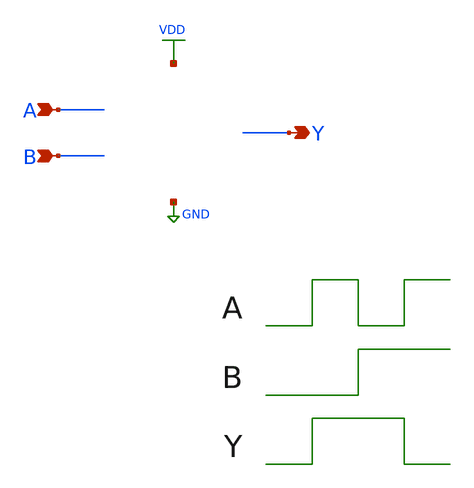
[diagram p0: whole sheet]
** sch_path: xor_test.sch
**.subckt xor_test A B Y
*.ipin A
*.ipin B
*.opin Y
**** begin user architecture code



VP VDD 0 dc 1.8

// XOR_A TEST

VA A 0 dc 0
VB B 0 dc 1.8

.control
save a b c d y
alter @va[PULSE] [ 1.8 0 1n 40p 40p 10n 20n ]
alter @vb[PULSE] [ 1.8 0 1n 40p 40p 20n 40n ]
tran 10p 60n
meas tran test1 FIND v(y) WHEN time=5n > NUL
meas tran test2 FIND v(y) WHEN time=15n > NUL
meas tran test3 FIND v(y) WHEN time=25n > NUL
meas tran test4 FIND v(y) WHEN time=35n > NUL
echo '*** TEST ***'
echo '-B--A--Y-'
echo -n '-L--L--'
if test1 >= 0.9
  echo 'H-'
else
  echo 'L-'
end
echo -n '-L--H--'
if test2 >= 0.9
  echo 'H-'
else
  echo 'L-'
end
echo -n '-H--L--'
if test3 >= 0.9
  echo 'H-'
else
  echo 'L-'
end
echo -n '-H--H--'
if test4 >= 0.9
  echo 'H-'
else
  echo 'L-'
end
.endc



 .param mc_mm_switch=0
.param mc_pr_switch=0
.include $::SKYWATER_MODELS/corners/tt.spice
.include $::SKYWATER_MODELS/r+c/res_typical__cap_typical.spice
.include $::SKYWATER_MODELS/r+c/res_typical__cap_typical__lin.spice
.include $::SKYWATER_MODELS/corners/tt/specialized_cells.spice
.include $::SKYWATER_STDCELLS/sky130_fd_sc_hd.spice

**** end user architecture code
**.ends
.GLOBAL VDD
.GLOBAL GND
.end
